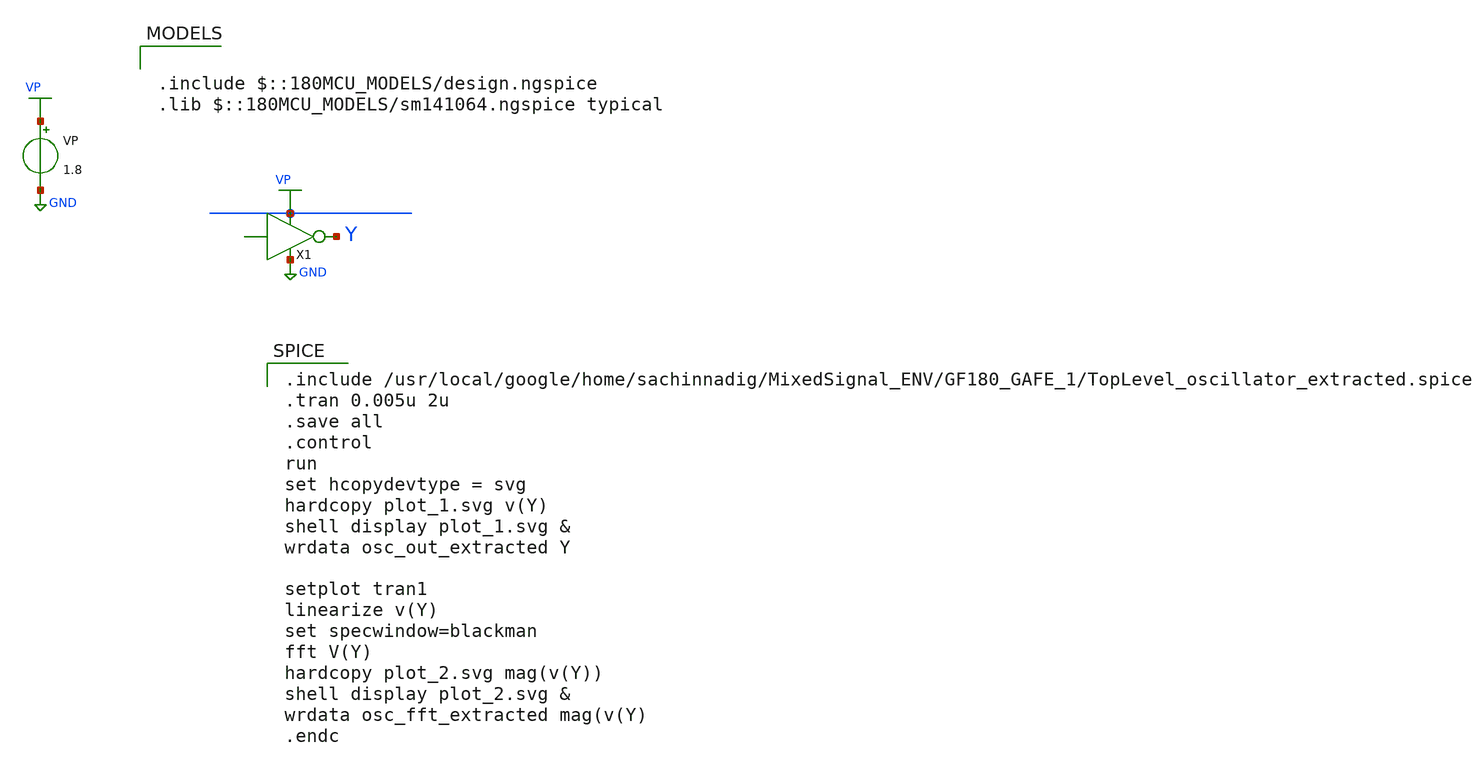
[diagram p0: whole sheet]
** sch_path: TopLevel_oscillator_extracted.sch
**.subckt TopLevel_oscillator_extracted
VP VP GND 1.8
X1 VP GND Y TopLevel_oscillator_extracted
**** begin user architecture code

.include $::180MCU_MODELS/design.ngspice
.lib $::180MCU_MODELS/sm141064.ngspice typical


.include /usr/local/google/home/sachinnadig/MixedSignal_ENV/GF180_GAFE_1/TopLevel_oscillator_extracted.spice
.tran 0.005u 2u
.save all
.control
run
set hcopydevtype = svg
hardcopy plot_1.svg v(Y)
shell display plot_1.svg &
wrdata osc_out_extracted Y

setplot tran1
linearize v(Y)
set specwindow=blackman
fft V(Y)
hardcopy plot_2.svg mag(v(Y))
shell display plot_2.svg &
wrdata osc_fft_extracted mag(v(Y)
.endc

**** end user architecture code
**.ends
.GLOBAL VP
.GLOBAL GND
.end
